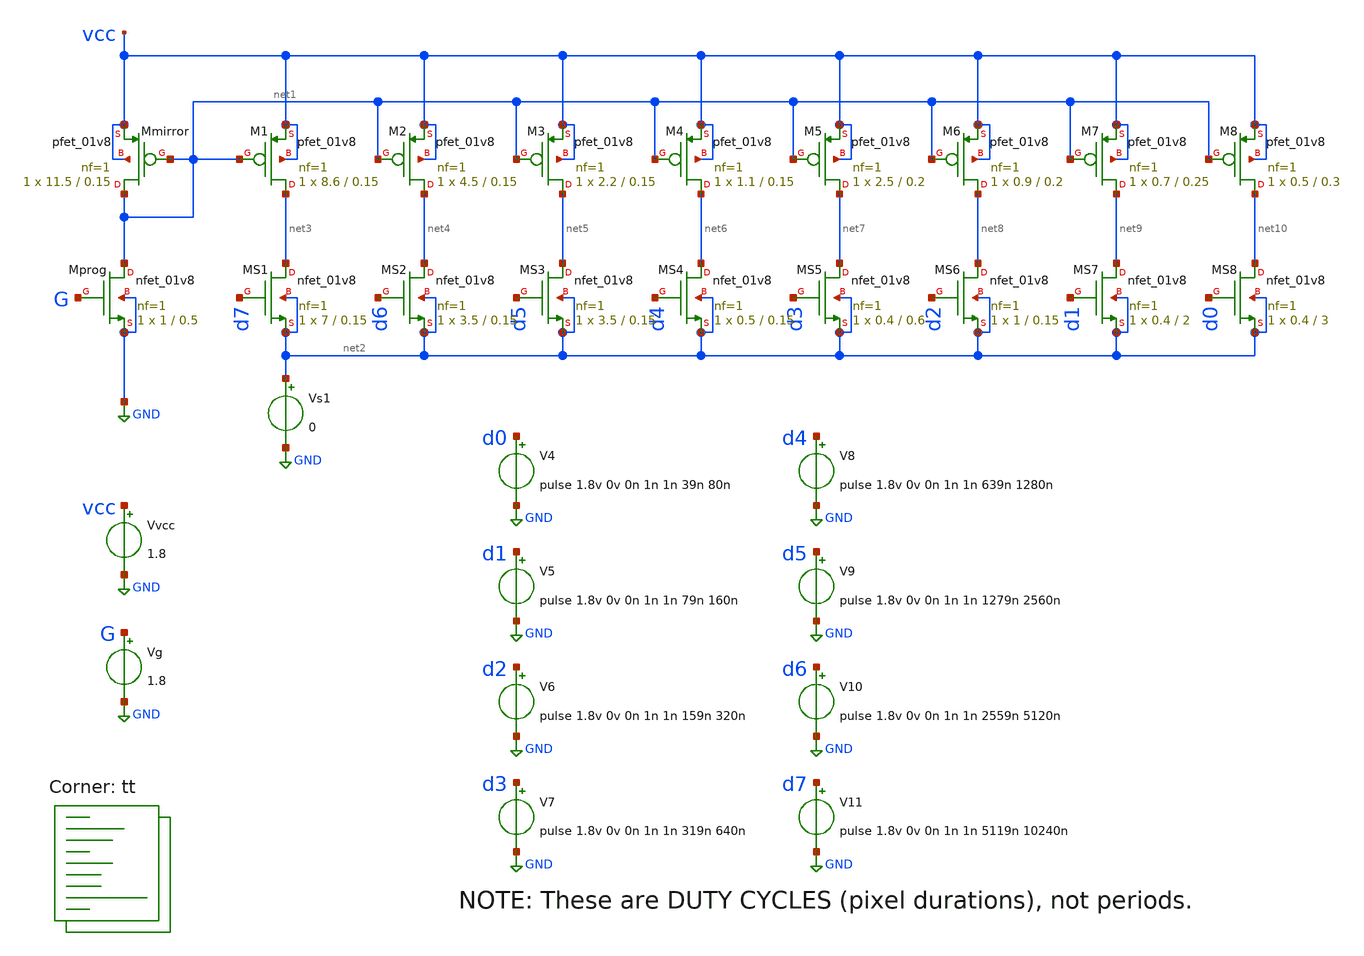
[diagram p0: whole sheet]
** sch_path: xschem/05-csdac2.sch
**.subckt 05-csdac2
Vvcc vcc GND 1.8
Vg G GND 1.8
XMprog net1 G GND GND sky130_fd_pr__nfet_01v8 L=0.5 W=1 nf=1 ad='int((nf+1)/2) * W/nf * 0.29' as='int((nf+2)/2) * W/nf * 0.29'
+ pd='2*int((nf+1)/2) * (W/nf + 0.29)' ps='2*int((nf+2)/2) * (W/nf + 0.29)' nrd='0.29 / W' nrs='0.29 / W'
+ sa=0 sb=0 sd=0 mult=1 m=1
XMmirror net1 net1 vcc vcc sky130_fd_pr__pfet_01v8 L=0.15 W=11.5 nf=1 ad='int((nf+1)/2) * W/nf * 0.29'
+ as='int((nf+2)/2) * W/nf * 0.29' pd='2*int((nf+1)/2) * (W/nf + 0.29)' ps='2*int((nf+2)/2) * (W/nf + 0.29)'
+ nrd='0.29 / W' nrs='0.29 / W' sa=0 sb=0 sd=0 mult=1 m=1
XM1 net3 net1 vcc vcc sky130_fd_pr__pfet_01v8 L=0.15 W=8.6 nf=1 ad='int((nf+1)/2) * W/nf * 0.29' as='int((nf+2)/2) * W/nf * 0.29'
+ pd='2*int((nf+1)/2) * (W/nf + 0.29)' ps='2*int((nf+2)/2) * (W/nf + 0.29)' nrd='0.29 / W' nrs='0.29 / W'
+ sa=0 sb=0 sd=0 mult=1 m=1
Vs1 net2 GND 0
XM2 net4 net1 vcc vcc sky130_fd_pr__pfet_01v8 L=0.15 W=4.5 nf=1 ad='int((nf+1)/2) * W/nf * 0.29' as='int((nf+2)/2) * W/nf * 0.29'
+ pd='2*int((nf+1)/2) * (W/nf + 0.29)' ps='2*int((nf+2)/2) * (W/nf + 0.29)' nrd='0.29 / W' nrs='0.29 / W'
+ sa=0 sb=0 sd=0 mult=1 m=1
XM3 net5 net1 vcc vcc sky130_fd_pr__pfet_01v8 L=0.15 W=2.2 nf=1 ad='int((nf+1)/2) * W/nf * 0.29' as='int((nf+2)/2) * W/nf * 0.29'
+ pd='2*int((nf+1)/2) * (W/nf + 0.29)' ps='2*int((nf+2)/2) * (W/nf + 0.29)' nrd='0.29 / W' nrs='0.29 / W'
+ sa=0 sb=0 sd=0 mult=1 m=1
XM4 net6 net1 vcc vcc sky130_fd_pr__pfet_01v8 L=0.15 W=1.1 nf=1 ad='int((nf+1)/2) * W/nf * 0.29' as='int((nf+2)/2) * W/nf * 0.29'
+ pd='2*int((nf+1)/2) * (W/nf + 0.29)' ps='2*int((nf+2)/2) * (W/nf + 0.29)' nrd='0.29 / W' nrs='0.29 / W'
+ sa=0 sb=0 sd=0 mult=1 m=1
XM5 net7 net1 vcc vcc sky130_fd_pr__pfet_01v8 L=0.2 W=2.5 nf=1 ad='int((nf+1)/2) * W/nf * 0.29' as='int((nf+2)/2) * W/nf * 0.29'
+ pd='2*int((nf+1)/2) * (W/nf + 0.29)' ps='2*int((nf+2)/2) * (W/nf + 0.29)' nrd='0.29 / W' nrs='0.29 / W'
+ sa=0 sb=0 sd=0 mult=1 m=1
XM6 net8 net1 vcc vcc sky130_fd_pr__pfet_01v8 L=0.2 W=0.9 nf=1 ad='int((nf+1)/2) * W/nf * 0.29' as='int((nf+2)/2) * W/nf * 0.29'
+ pd='2*int((nf+1)/2) * (W/nf + 0.29)' ps='2*int((nf+2)/2) * (W/nf + 0.29)' nrd='0.29 / W' nrs='0.29 / W'
+ sa=0 sb=0 sd=0 mult=1 m=1
XM7 net9 net1 vcc vcc sky130_fd_pr__pfet_01v8 L=0.25 W=0.7 nf=1 ad='int((nf+1)/2) * W/nf * 0.29' as='int((nf+2)/2) * W/nf * 0.29'
+ pd='2*int((nf+1)/2) * (W/nf + 0.29)' ps='2*int((nf+2)/2) * (W/nf + 0.29)' nrd='0.29 / W' nrs='0.29 / W'
+ sa=0 sb=0 sd=0 mult=1 m=1
XM8 net10 net1 vcc vcc sky130_fd_pr__pfet_01v8 L=0.3 W=0.5 nf=1 ad='int((nf+1)/2) * W/nf * 0.29' as='int((nf+2)/2) * W/nf * 0.29'
+ pd='2*int((nf+1)/2) * (W/nf + 0.29)' ps='2*int((nf+2)/2) * (W/nf + 0.29)' nrd='0.29 / W' nrs='0.29 / W'
+ sa=0 sb=0 sd=0 mult=1 m=1
XMS1 net3 d7 net2 net2 sky130_fd_pr__nfet_01v8 L=0.15 W=7 nf=1 ad='int((nf+1)/2) * W/nf * 0.29' as='int((nf+2)/2) * W/nf * 0.29'
+ pd='2*int((nf+1)/2) * (W/nf + 0.29)' ps='2*int((nf+2)/2) * (W/nf + 0.29)' nrd='0.29 / W' nrs='0.29 / W'
+ sa=0 sb=0 sd=0 mult=1 m=1
XMS2 net4 d6 net2 net2 sky130_fd_pr__nfet_01v8 L=0.15 W=3.5 nf=1 ad='int((nf+1)/2) * W/nf * 0.29' as='int((nf+2)/2) * W/nf * 0.29'
+ pd='2*int((nf+1)/2) * (W/nf + 0.29)' ps='2*int((nf+2)/2) * (W/nf + 0.29)' nrd='0.29 / W' nrs='0.29 / W'
+ sa=0 sb=0 sd=0 mult=1 m=1
XMS3 net5 d5 net2 net2 sky130_fd_pr__nfet_01v8 L=0.15 W=3.5 nf=1 ad='int((nf+1)/2) * W/nf * 0.29' as='int((nf+2)/2) * W/nf * 0.29'
+ pd='2*int((nf+1)/2) * (W/nf + 0.29)' ps='2*int((nf+2)/2) * (W/nf + 0.29)' nrd='0.29 / W' nrs='0.29 / W'
+ sa=0 sb=0 sd=0 mult=1 m=1
XMS4 net6 d4 net2 net2 sky130_fd_pr__nfet_01v8 L=0.15 W=0.5 nf=1 ad='int((nf+1)/2) * W/nf * 0.29' as='int((nf+2)/2) * W/nf * 0.29'
+ pd='2*int((nf+1)/2) * (W/nf + 0.29)' ps='2*int((nf+2)/2) * (W/nf + 0.29)' nrd='0.29 / W' nrs='0.29 / W'
+ sa=0 sb=0 sd=0 mult=1 m=1
XMS5 net7 d3 net2 net2 sky130_fd_pr__nfet_01v8 L=0.6 W=0.4 nf=1 ad='int((nf+1)/2) * W/nf * 0.29' as='int((nf+2)/2) * W/nf * 0.29'
+ pd='2*int((nf+1)/2) * (W/nf + 0.29)' ps='2*int((nf+2)/2) * (W/nf + 0.29)' nrd='0.29 / W' nrs='0.29 / W'
+ sa=0 sb=0 sd=0 mult=1 m=1
XMS6 net8 d2 net2 net2 sky130_fd_pr__nfet_01v8 L=0.15 W=1 nf=1 ad='int((nf+1)/2) * W/nf * 0.29' as='int((nf+2)/2) * W/nf * 0.29'
+ pd='2*int((nf+1)/2) * (W/nf + 0.29)' ps='2*int((nf+2)/2) * (W/nf + 0.29)' nrd='0.29 / W' nrs='0.29 / W'
+ sa=0 sb=0 sd=0 mult=1 m=1
XMS7 net9 d1 net2 net2 sky130_fd_pr__nfet_01v8 L=2 W=0.4 nf=1 ad='int((nf+1)/2) * W/nf * 0.29' as='int((nf+2)/2) * W/nf * 0.29'
+ pd='2*int((nf+1)/2) * (W/nf + 0.29)' ps='2*int((nf+2)/2) * (W/nf + 0.29)' nrd='0.29 / W' nrs='0.29 / W'
+ sa=0 sb=0 sd=0 mult=1 m=1
XMS8 net10 d0 net2 net2 sky130_fd_pr__nfet_01v8 L=3 W=0.4 nf=1 ad='int((nf+1)/2) * W/nf * 0.29' as='int((nf+2)/2) * W/nf * 0.29'
+ pd='2*int((nf+1)/2) * (W/nf + 0.29)' ps='2*int((nf+2)/2) * (W/nf + 0.29)' nrd='0.29 / W' nrs='0.29 / W'
+ sa=0 sb=0 sd=0 mult=1 m=1
V4 d0 GND pulse 1.8v 0v 0n 1n 1n 39n 80n
V5 d1 GND pulse 1.8v 0v 0n 1n 1n 79n 160n
V6 d2 GND pulse 1.8v 0v 0n 1n 1n 159n 320n
V7 d3 GND pulse 1.8v 0v 0n 1n 1n 319n 640n
V8 d4 GND pulse 1.8v 0v 0n 1n 1n 639n 1280n
V9 d5 GND pulse 1.8v 0v 0n 1n 1n 1279n 2560n
V10 d6 GND pulse 1.8v 0v 0n 1n 1n 2559n 5120n
V11 d7 GND pulse 1.8v 0v 0n 1n 1n 5119n 10240n
**** begin user architecture code



.options savecurrents
.control

  save all
  tran 1n 12.8u
  write 05.raw i(Vs1)

.endc



.lib $::SKYWATER_MODELS/sky130.lib.spice tt
**** end user architecture code
**.ends
.GLOBAL GND
.end
